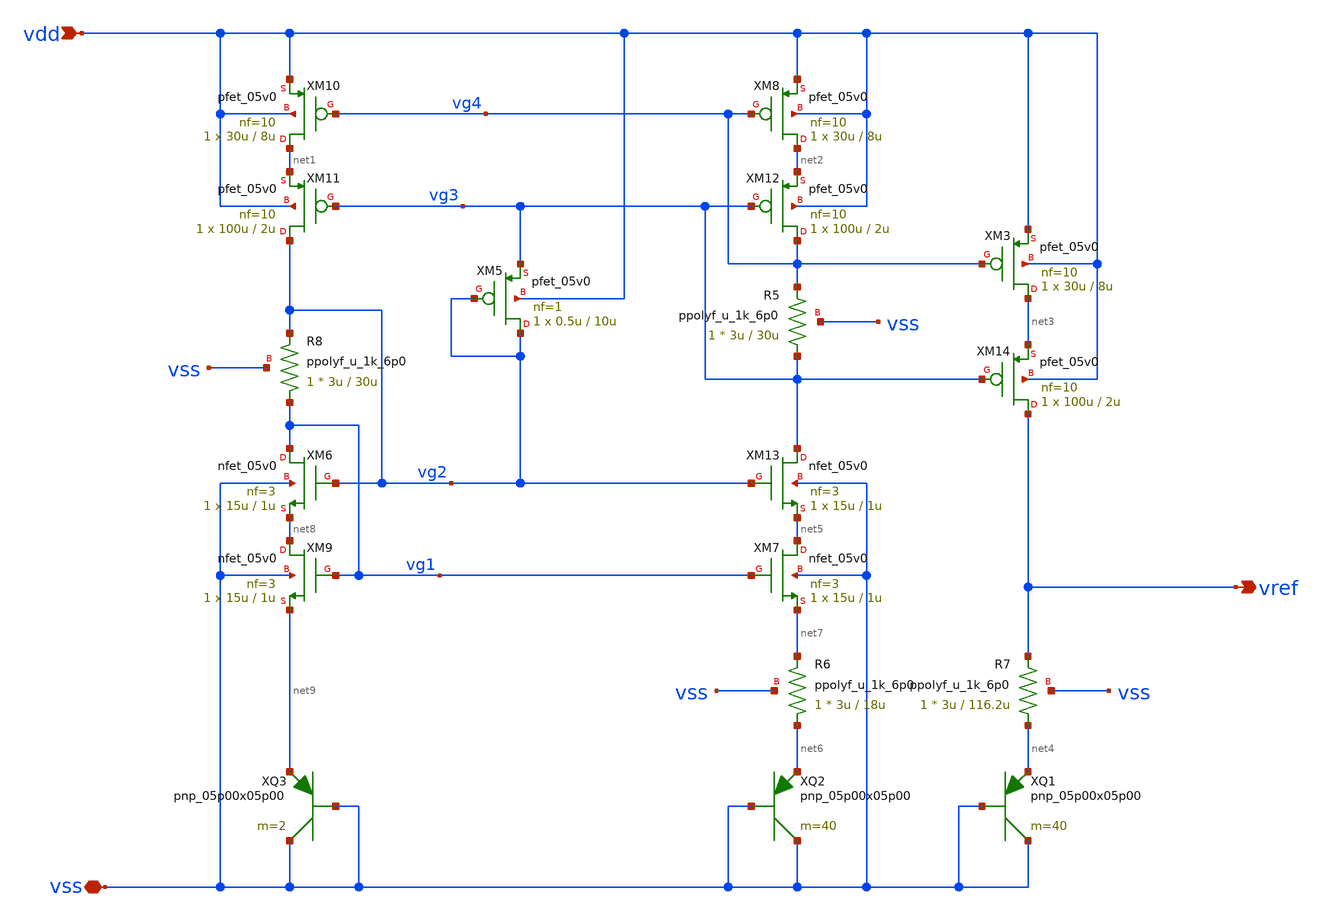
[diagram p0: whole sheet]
** sch_path: xschem_main_gnssl1/bandgap.sch
**.subckt bandgap vdd vss vref
*.ipin vdd
*.iopin vss
*.opin vref
XQ1 vss vss net4 pnp_05p00x05p00 m=40 par=40
XQ2 vss vss net6 pnp_05p00x05p00 m=40 par=40
XQ3 vss vss net9 pnp_05p00x05p00 m=2 par=2
XM8 net2 vg4 vdd vdd pfet_05v0 L=8u W=30u nf=10 ad='int((nf+1)/2) * W/nf * 0.18u' as='int((nf+2)/2) * W/nf * 0.18u'
+ pd='2*int((nf+1)/2) * (W/nf + 0.18u)' ps='2*int((nf+2)/2) * (W/nf + 0.18u)' nrd='0.18u / W' nrs='0.18u / W'
+ sa=0 sb=0 sd=0 m=1
XM13 vg3 vg2 net5 vss nfet_05v0 L=1u W=15u nf=3 ad='int((nf+1)/2) * W/nf * 0.18u' as='int((nf+2)/2) * W/nf * 0.18u'
+ pd='2*int((nf+1)/2) * (W/nf + 0.18u)' ps='2*int((nf+2)/2) * (W/nf + 0.18u)' nrd='0.18u / W' nrs='0.18u / W'
+ sa=0 sb=0 sd=0 m=1
XM10 net1 vg4 vdd vdd pfet_05v0 L=8u W=30u nf=10 ad='int((nf+1)/2) * W/nf * 0.18u' as='int((nf+2)/2) * W/nf * 0.18u'
+ pd='2*int((nf+1)/2) * (W/nf + 0.18u)' ps='2*int((nf+2)/2) * (W/nf + 0.18u)' nrd='0.18u / W' nrs='0.18u / W'
+ sa=0 sb=0 sd=0 m=1
XM11 vg2 vg3 net1 vdd pfet_05v0 L=2u W=100u nf=10 ad='int((nf+1)/2) * W/nf * 0.18u' as='int((nf+2)/2) * W/nf * 0.18u'
+ pd='2*int((nf+1)/2) * (W/nf + 0.18u)' ps='2*int((nf+2)/2) * (W/nf + 0.18u)' nrd='0.18u / W' nrs='0.18u / W'
+ sa=0 sb=0 sd=0 m=1
XM12 vg4 vg3 net2 vdd pfet_05v0 L=2u W=100u nf=10 ad='int((nf+1)/2) * W/nf * 0.18u' as='int((nf+2)/2) * W/nf * 0.18u'
+ pd='2*int((nf+1)/2) * (W/nf + 0.18u)' ps='2*int((nf+2)/2) * (W/nf + 0.18u)' nrd='0.18u / W' nrs='0.18u / W'
+ sa=0 sb=0 sd=0 m=1
XM3 net3 vg4 vdd vdd pfet_05v0 L=8u W=30u nf=10 ad='int((nf+1)/2) * W/nf * 0.18u' as='int((nf+2)/2) * W/nf * 0.18u'
+ pd='2*int((nf+1)/2) * (W/nf + 0.18u)' ps='2*int((nf+2)/2) * (W/nf + 0.18u)' nrd='0.18u / W' nrs='0.18u / W'
+ sa=0 sb=0 sd=0 m=1
XM14 vref vg3 net3 vdd pfet_05v0 L=2u W=100u nf=10 ad='int((nf+1)/2) * W/nf * 0.18u' as='int((nf+2)/2) * W/nf * 0.18u'
+ pd='2*int((nf+1)/2) * (W/nf + 0.18u)' ps='2*int((nf+2)/2) * (W/nf + 0.18u)' nrd='0.18u / W' nrs='0.18u / W'
+ sa=0 sb=0 sd=0 m=1
XM5 vg2 vg2 vg3 vdd pfet_05v0 L=10u W=0.5u nf=1 ad='int((nf+1)/2) * W/nf * 0.18u' as='int((nf+2)/2) * W/nf * 0.18u'
+ pd='2*int((nf+1)/2) * (W/nf + 0.18u)' ps='2*int((nf+2)/2) * (W/nf + 0.18u)' nrd='0.18u / W' nrs='0.18u / W'
+ sa=0 sb=0 sd=0 m=1
XM6 vg1 vg2 net8 vss nfet_05v0 L=1u W=15u nf=3 ad='int((nf+1)/2) * W/nf * 0.18u' as='int((nf+2)/2) * W/nf * 0.18u'
+ pd='2*int((nf+1)/2) * (W/nf + 0.18u)' ps='2*int((nf+2)/2) * (W/nf + 0.18u)' nrd='0.18u / W' nrs='0.18u / W'
+ sa=0 sb=0 sd=0 m=1
XM9 net8 vg1 net9 vss nfet_05v0 L=1u W=15u nf=3 ad='int((nf+1)/2) * W/nf * 0.18u' as='int((nf+2)/2) * W/nf * 0.18u'
+ pd='2*int((nf+1)/2) * (W/nf + 0.18u)' ps='2*int((nf+2)/2) * (W/nf + 0.18u)' nrd='0.18u / W' nrs='0.18u / W'
+ sa=0 sb=0 sd=0 m=1
XM7 net5 vg1 net7 vss nfet_05v0 L=1u W=15u nf=3 ad='int((nf+1)/2) * W/nf * 0.18u' as='int((nf+2)/2) * W/nf * 0.18u'
+ pd='2*int((nf+1)/2) * (W/nf + 0.18u)' ps='2*int((nf+2)/2) * (W/nf + 0.18u)' nrd='0.18u / W' nrs='0.18u / W'
+ sa=0 sb=0 sd=0 m=1
XR6 net6 net7 vss ppolyf_u_1k_6p0 r_width=3u r_length=18u m=1
XR7 net4 vref vss ppolyf_u_1k_6p0 r_width=3u r_length=116.2u m=1
XR8 vg1 vg2 vss ppolyf_u_1k_6p0 r_width=3u r_length=30u m=1
XR5 vg3 vg4 vss ppolyf_u_1k_6p0 r_width=3u r_length=30u m=1
**.ends
.end
